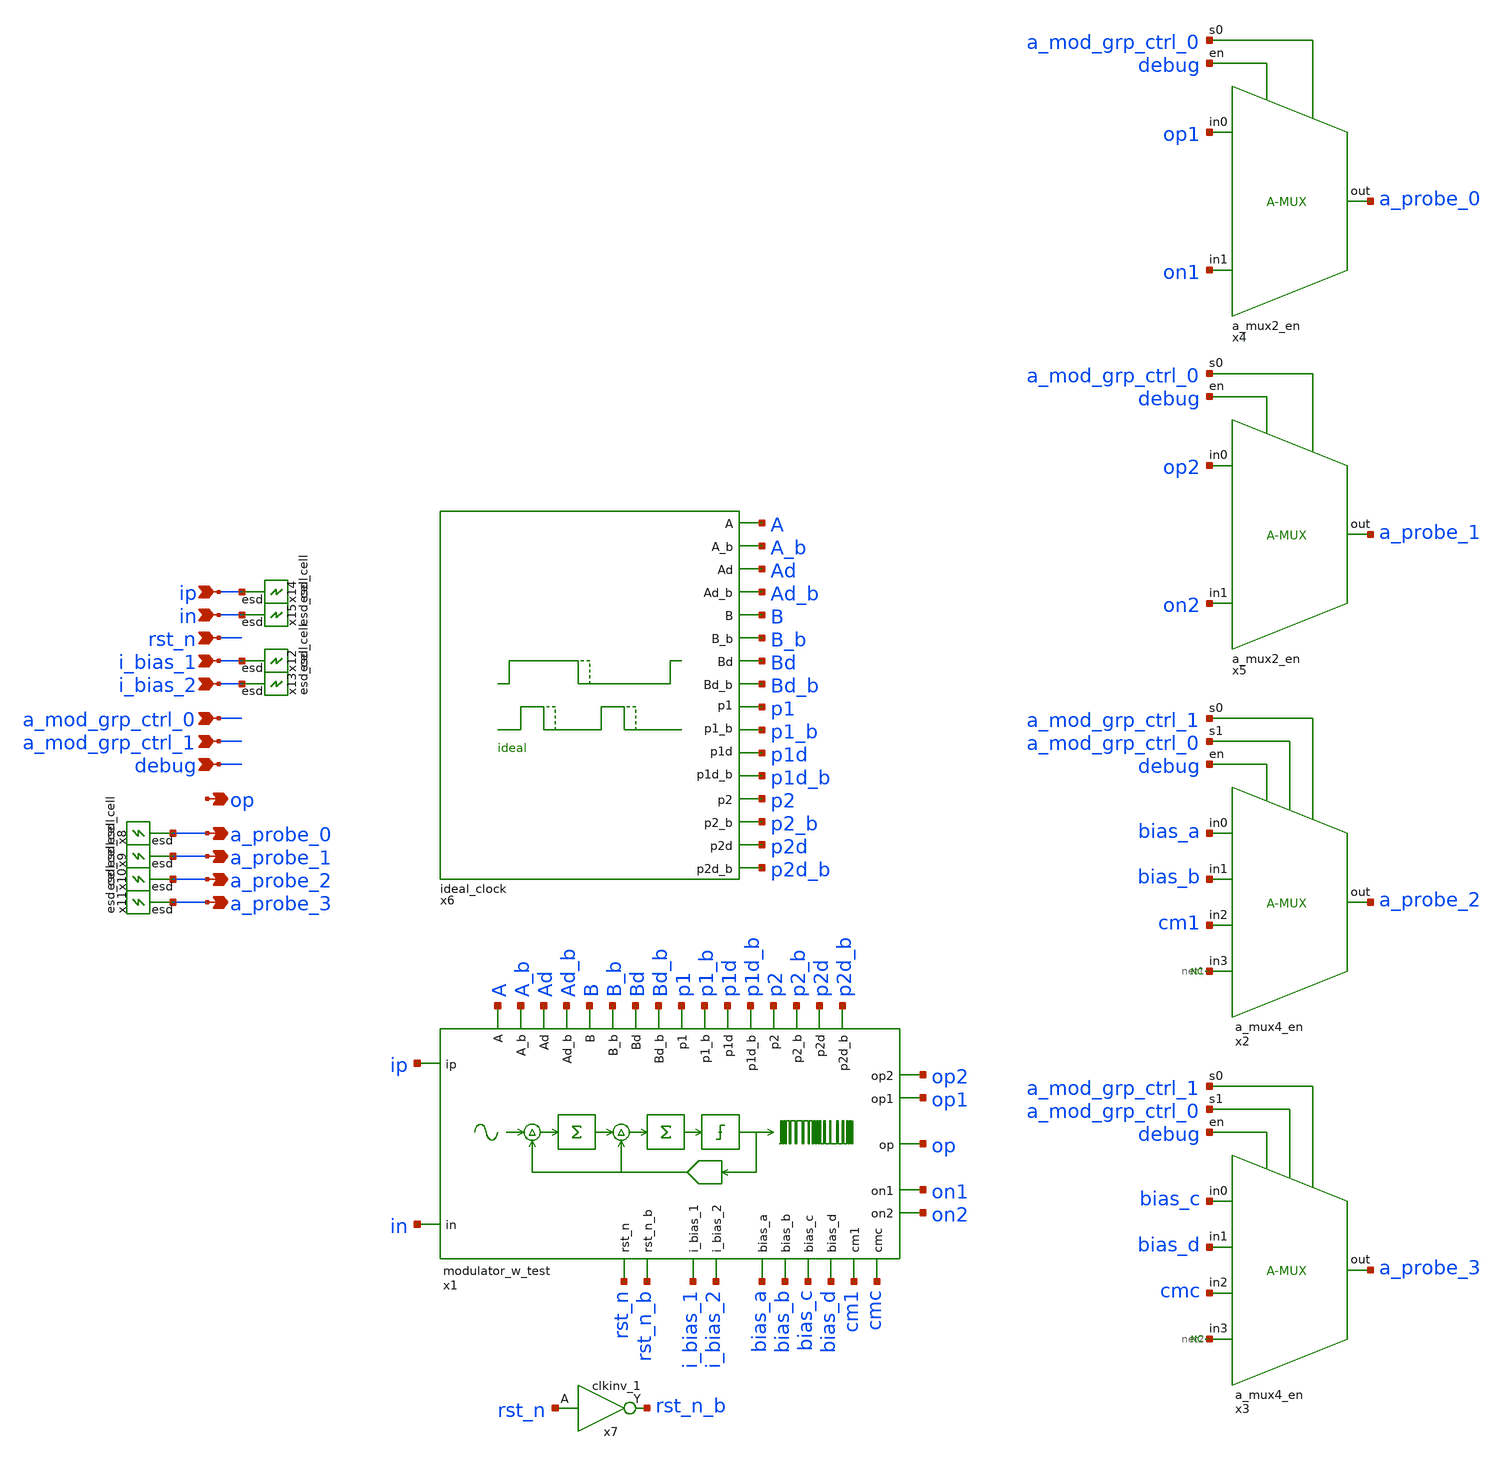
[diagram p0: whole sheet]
** sch_path: design/analog_modulator/schematic/analog_top_ideal_clock.sch
**.subckt analog_top_ideal_clock ip in rst_n i_bias_1 i_bias_2 a_mod_grp_ctrl_0 a_mod_grp_ctrl_1
*+ debug op a_probe_0 a_probe_1 a_probe_2 a_probe_3
*.ipin ip
*.ipin in
*.ipin rst_n
*.ipin i_bias_1
*.ipin i_bias_2
*.ipin a_mod_grp_ctrl_0
*.ipin a_mod_grp_ctrl_1
*.ipin debug
*.opin op
*.opin a_probe_0
*.opin a_probe_1
*.opin a_probe_2
*.opin a_probe_3
x1 ip in A A_b Ad Ad_b B B_b Bd Bd_b p1 p1_b p1d p1d_b p2 p2_b p2d p2d_b rst_n rst_n_b i_bias_1
+ i_bias_2 op bias_a bias_b bias_c bias_d cm1 cmc op2 op1 on1 on2 VDD VSS modulator_w_test
x2 a_mod_grp_ctrl_1 a_mod_grp_ctrl_0 debug bias_a bias_b cm1 net1 a_probe_2 VDD VSS a_mux4_en
* noconn #net1
x3 a_mod_grp_ctrl_1 a_mod_grp_ctrl_0 debug bias_c bias_d cmc net2 a_probe_3 VDD VSS a_mux4_en
* noconn #net2
x4 a_mod_grp_ctrl_0 debug op1 on1 a_probe_0 VDD VSS a_mux2_en
x5 a_mod_grp_ctrl_0 debug op2 on2 a_probe_1 VDD VSS a_mux2_en
x7 rst_n VSS VSS VDD VDD rst_n_b sky130_fd_sc_hd__clkinv_1
x8 a_probe_0 VDD VSS esd_cell
x9 a_probe_1 VDD VSS esd_cell
x10 a_probe_2 VDD VSS esd_cell
x11 a_probe_3 VDD VSS esd_cell
x12 i_bias_1 VDD VSS esd_cell
x13 i_bias_2 VDD VSS esd_cell
x14 ip VDD VSS esd_cell
x15 in VDD VSS esd_cell
x6 A A_b Ad Ad_b Bd_b Bd B_b B p2 p2_b p2d p2d_b p1d_b p1d p1_b p1 VDD VSS ideal_clock td=0
**.ends
.end
